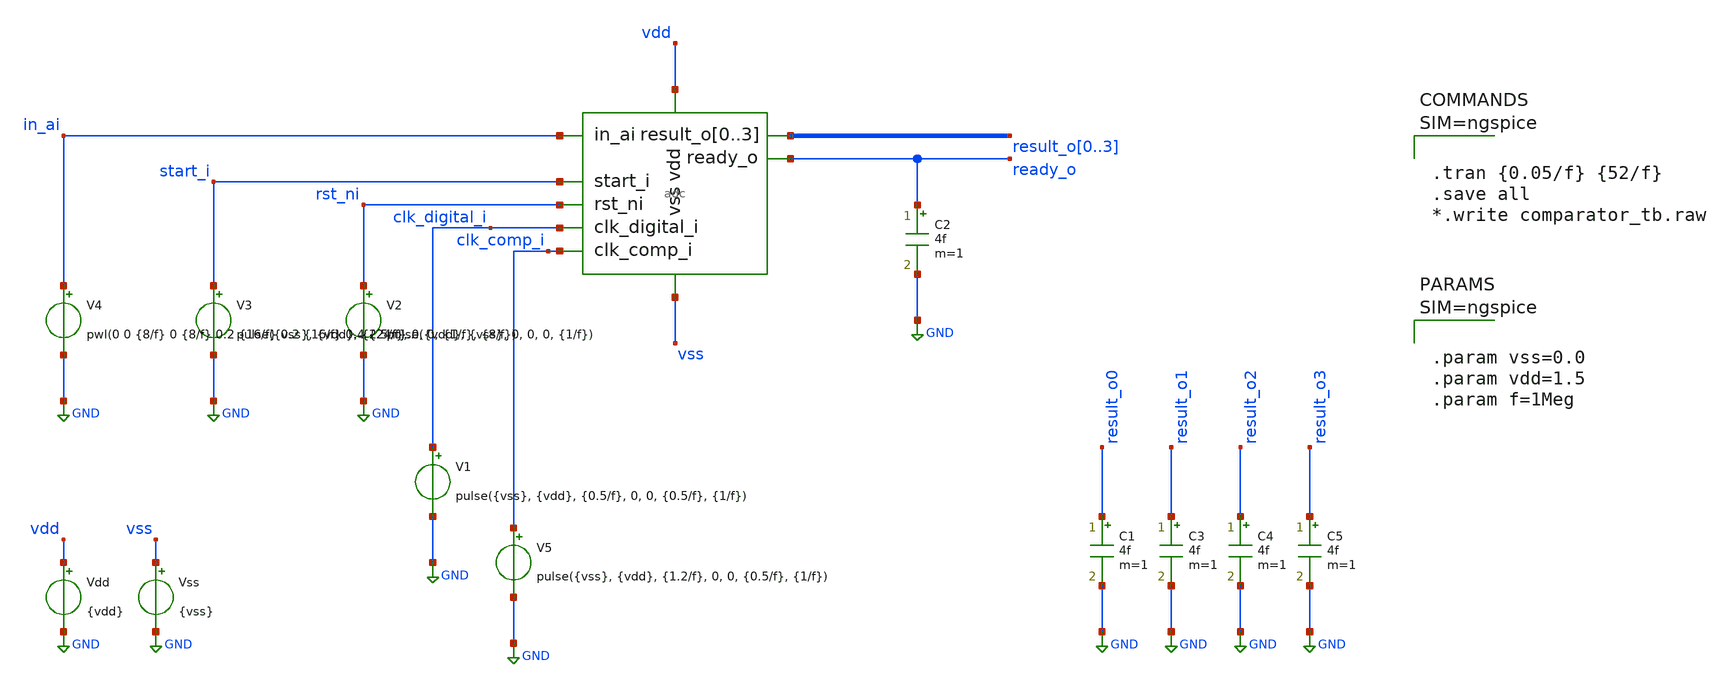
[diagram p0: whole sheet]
** sch_path: designs/basic1/adc_tb.sch
* IHP-GmbH/IHP-Open-PDK/ihp-sg13g2/libs.tech/xschem/sg13g2_stdcells/sg13g2_inv_2.sch:
* Copyright 2023 IHP PDK Authors
* Licensed under the Apache License, Version 2.0 (the "License");
**.subckt adc_tb
x1 in_ai start_i rst_ni clk_digital_i result_o0 result_o1 result_o2 result_o3 ready_o vdd vss
+ clk_comp_i adc
V1 clk_digital_i GND pulse({vss}, {vdd}, {0.5/f}, 0, 0, {0.5/f}, {1/f})
V2 rst_ni GND pulse({vdd}, {vss}, 0, 0, 0, {1/f})
V3 start_i GND pulse({vss}, {vdd}, {2.5/f}, 0, 0, {1/f}, {8/f})
V4 in_ai GND pwl(0 0 {8/f} 0 {8/f} 0.2 {16/f} 0.2 {16/f} 0.4 {24/f} 0.4 {24/f} 0.6 {32/f} 0.6 {32/f}
+ 0.8 {40/f} 0.8 {40/f} 1.0 {52/f} 1.0)
.save i(v4)
Vdd vdd GND {vdd}
Vss vss GND {vss}
C1 result_o0 GND 4f m=1
C2 ready_o GND 4f m=1
C3 result_o1 GND 4f m=1
C4 result_o2 GND 4f m=1
C5 result_o3 GND 4f m=1
V5 clk_comp_i GND pulse({vss}, {vdd}, {1.2/f}, 0, 0, {0.5/f}, {1/f})
**** begin user architecture code

.lib $::SG13G2_MODELS/cornerMOSlv.lib mos_tt
.lib $::SG13G2_MODELS/cornerCAP.lib cap_typ
.include $::PDK_ROOT/ihp-sg13g2/libs.ref/sg13g2_stdcell/spice/sg13g2_stdcell.spice




.tran {0.05/f} {52/f}
.save all
*.write comparator_tb.raw






.param vss=0.0
.param vdd=1.5
.param f=1Meg






.model adc_buff_clk adc_bridge(in_low = 'vdd/2' in_high = 'vdd/2')

.control
pre_set auto_bridge_d_out =  ( ".model auto_bridge_out bidi_bridge(direction=0 out_high=1.5
+ t_rise=1n t_fall=1n)"    "auto_bridge_out%d [ %s ] [ %s ] null auto_bridge_out" )
pre_set auto_bridge_d_in =  ( ".model auto_bridge_in bidi_bridge(direction=1 in_low=0.5 in_high=1)"
+    "auto_bridge_in%d [ %s ] [ %s ] null auto_bridge_in" )
.endc



**** end user architecture code
**.ends

* expanding   symbol:  adc.sym # of pins=9
** sym_path: designs/basic1/adc.sym
** sch_path: designs/basic1/adc.sch
.subckt adc in_ai start_i rst_ni clk_digital_i result_o0 result_o1 result_o2 result_o3 ready_o vdd
+ vss clk_comp_i
*.ipin in_ai
*.ipin clk_digital_i
*.ipin vss
*.ipin vdd
*.ipin rst_ni
*.ipin start_i
*.opin ready_o
*.opin result_o0,result_o1,result_o2,result_o3
*.ipin clk_comp_i
x3 sample dac_o0 dac_o1 dac_o2 dac_o3 dac_o0 dac_o1 dac_o2 dac_o3 vss vdd cdac
A2 [ clk_digital_i ] [ net1 ] adc_buff_clk
A1 [ net1 start_i rst_ni comp ] [ ready_o sample_o dac_o0 dac_o1 dac_o2 dac_o3 result_o0 result_o1
+ result_o2 result_o3 ] adc
A3 [ %vd(sample vdd) ] [ comp ] comp
A4 [ comp ] [ comp_a ] dac_buff
* noconn %vd(sample vdd)
* noconn clk_comp_i
.ends


* expanding   symbol:  /workspaces/ngspice_cosim_inv/designs/cdac/cdac.sym # of pins=4
** sym_path: designs/cdac/cdac.sym
** sch_path: designs/cdac/cdac.sch
.subckt cdac VIN CTRL0 CTRL1 CTRL2 CTRL3 CTRL4 CTRL5 CTRL6 CTRL7 VSS VDD
*.ipin VIN
*.ipin CTRL0,CTRL1,CTRL2,CTRL3,CTRL4,CTRL5,CTRL6,CTRL7
*.ipin VSS
*.ipin VDD
XC2 VIN l1 cap_cmim w=7.297e-5 l=7.298e-5 m=1 mm_ok=1
XC3 VIN l2 cap_cmim w=5.158e-5 l=5.159e-5 m=1 mm_ok=1
XC4 VIN l3 cap_cmim w=3.646e-5 l=3.646e-5 m=1 mm_ok=1
XC5 VIN VSS cap_cmim w=6.402e-6 l=6.402e-6 m=1 mm_ok=1
x1 l1 CTRL0 VDD VSS sg13g2_inv_2
x2 l2 CTRL1 VDD VSS sg13g2_inv_2
x3 l3 CTRL2 VDD VSS sg13g2_inv_2
x4 l4 CTRL3 VDD VSS sg13g2_inv_2
XC6 VIN l4 cap_cmim w=2.577e-5 l=2.577e-5 m=1 mm_ok=1
XC7 VIN l5 cap_cmim w=1.820e-5 l=1.820e-5 m=1 mm_ok=1
XC8 VIN l6 cap_cmim w=1.286e-5 l=1.286e-5 m=1 mm_ok=1
XC9 VIN l7 cap_cmim w=9.077e-6 l=9.077e-6 m=1 mm_ok=1
x5 l5 CTRL4 VDD VSS sg13g2_inv_2
x6 l6 CTRL5 VDD VSS sg13g2_inv_2
x7 l7 CTRL6 VDD VSS sg13g2_inv_2
x8 l8 CTRL7 VDD VSS sg13g2_inv_2
XC1 VIN l8 cap_cmim w=6.402e-6 l=6.402e-6 m=1 mm_ok=1
.ends


* expanding   symbol:  sg13g2_stdcells/sg13g2_inv_2.sym # of pins=2
** sym_path: sg13g2_stdcells/sg13g2_inv_2.sym
** sch_path: sg13g2_stdcells/sg13g2_inv_2.sch
.subckt sg13g2_inv_2 Y A VDD VSS
*.opin Y
*.ipin A
*.iopin VDD
*.iopin VSS
XM1 Y A VSS VSS sg13_lv_nmos w=1.48u l=130.00n ng=2 m=1 mm_ok=1
XM2 Y A VDD VDD sg13_lv_pmos w=2.24u l=130.00n ng=2 m=1 mm_ok=1
.ends

.GLOBAL GND
**** begin user architecture code
.model adc d_cosim simulation="ivlng" sim_args=["adc"]
.model dac_buff dac_bridge input_load=1e-15 t_rise=10n t_fall=10n  out_low=0 out_high=1.5
.model comp adc_bridge in_low=0 in_high=0
**** end user architecture code
.end
